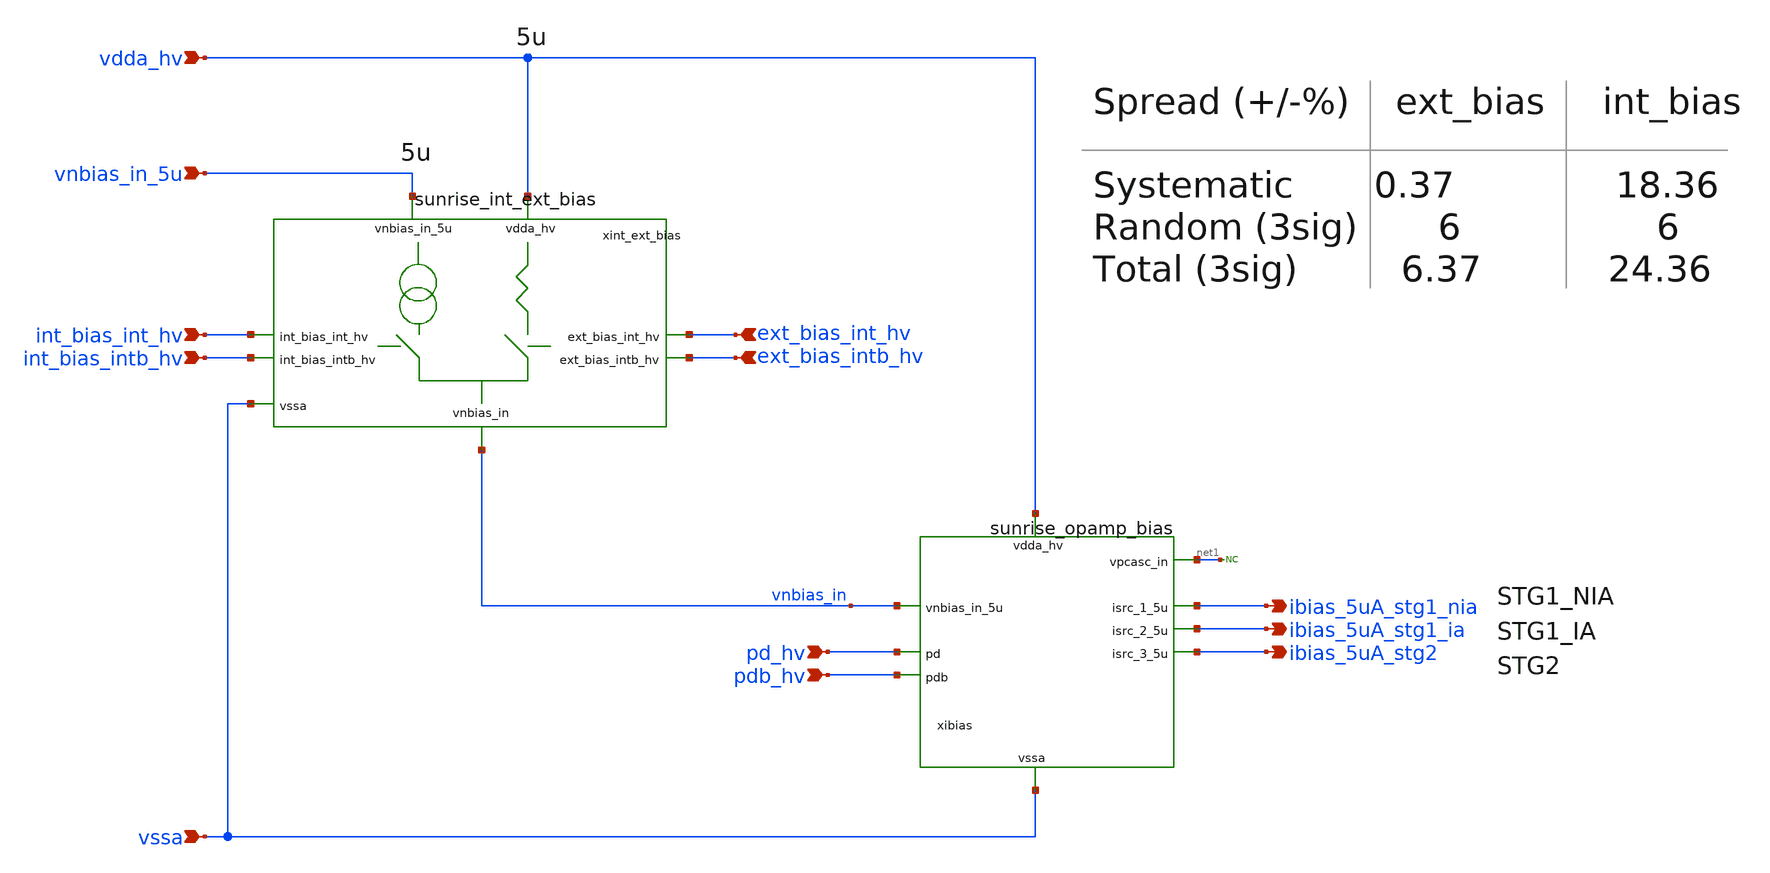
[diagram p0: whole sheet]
** sch_path: Schematics_Layout/sunrise_bias/sunrise_bias.sch
**.subckt sunrise_bias vssa vdda_hv ibias_5uA_stg1_nia ibias_5uA_stg1_ia ibias_5uA_stg2 pdb_hv pd_hv
*+ vnbias_in_5u ext_bias_intb_hv ext_bias_int_hv int_bias_int_hv int_bias_intb_hv
*.ipin vssa
*.ipin vdda_hv
*.opin ibias_5uA_stg1_nia
*.opin ibias_5uA_stg1_ia
*.opin ibias_5uA_stg2
*.ipin pdb_hv
*.ipin pd_hv
*.ipin vnbias_in_5u
*.ipin ext_bias_intb_hv
*.ipin ext_bias_int_hv
*.ipin int_bias_int_hv
*.ipin int_bias_intb_hv
xibias vdda_hv pdb_hv vnbias_in ibias_5uA_stg1_nia net1 pd_hv vssa ibias_5uA_stg1_ia ibias_5uA_stg2
+ sunrise_opamp_bias
* noconn #net1
xint_ext_bias vdda_hv vnbias_in_5u ext_bias_int_hv int_bias_intb_hv int_bias_int_hv ext_bias_intb_hv
+ vssa vnbias_in sunrise_int_ext_bias
**.ends
.end
